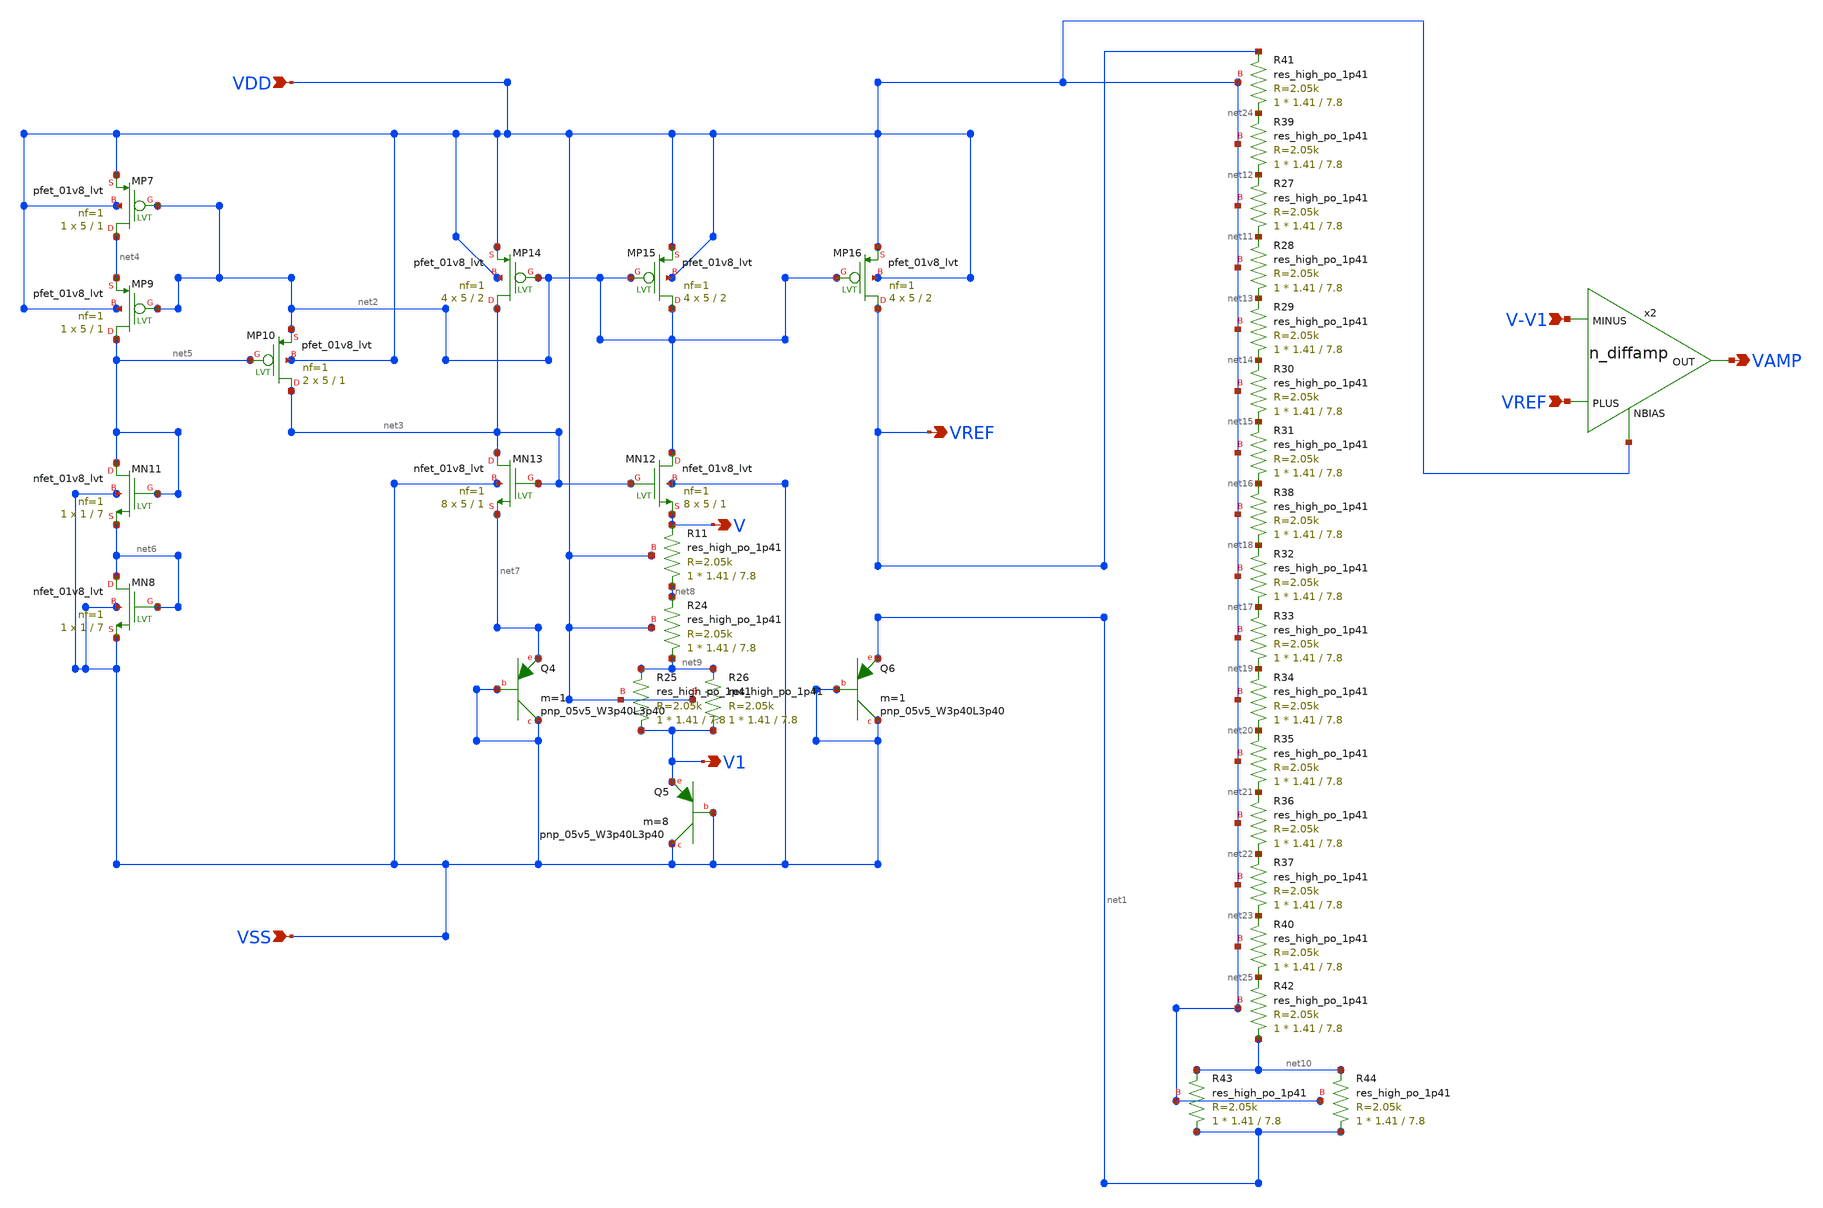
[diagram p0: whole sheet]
** sch_path: rply_project_sky130nm/design/RPLY_PROJECT_SKY130NM/RPLY_PROJECT.sch
* StefanSchippers/xschem_sky130/sky130_tests/n_diffamp.sch:
* Copyright 2021 Stefan Frederik Schippers
* Licensed under the Apache License, Version 2.0 (the "License");
**.subckt RPLY_PROJECT VDD VSS V-V1 VAMP V V1 VREF VREF
*.ipin VDD
*.ipin VSS
*.ipin V-V1
*.opin VAMP
*.opin V
*.opin V1
*.opin VREF
*.ipin VREF
XMP7 net4 net2 VDD VDD sky130_fd_pr__pfet_01v8_lvt L=1 W=5 nf=1 ad='int((nf+1)/2) * W/nf * 0.29' as='int((nf+2)/2) * W/nf * 0.29'
+ pd='2*int((nf+1)/2) * (W/nf + 0.29)' ps='2*int((nf+2)/2) * (W/nf + 0.29)' nrd='0.29 / W' nrs='0.29 / W'
+ sa=0 sb=0 sd=0 mult=1 m=1
XMN8 net6 net6 VSS VSS sky130_fd_pr__nfet_01v8_lvt L=7 W=1 nf=1 ad='int((nf+1)/2) * W/nf * 0.29' as='int((nf+2)/2) * W/nf * 0.29'
+ pd='2*int((nf+1)/2) * (W/nf + 0.29)' ps='2*int((nf+2)/2) * (W/nf + 0.29)' nrd='0.29 / W' nrs='0.29 / W'
+ sa=0 sb=0 sd=0 mult=1 m=1
XR11 net8 V VDD sky130_fd_pr__res_high_po_1p41 L=7.8 mult=1 m=1
XQ4 VSS VSS net7 sky130_fd_pr__pnp_05v5_W3p40L3p40 m=1
XMP9 net5 net2 net4 VDD sky130_fd_pr__pfet_01v8_lvt L=1 W=5 nf=1 ad='int((nf+1)/2) * W/nf * 0.29' as='int((nf+2)/2) * W/nf * 0.29'
+ pd='2*int((nf+1)/2) * (W/nf + 0.29)' ps='2*int((nf+2)/2) * (W/nf + 0.29)' nrd='0.29 / W' nrs='0.29 / W'
+ sa=0 sb=0 sd=0 mult=1 m=1
XMP10 net3 net5 net2 VDD sky130_fd_pr__pfet_01v8_lvt L=1 W=5 nf=1 ad='int((nf+1)/2) * W/nf * 0.29' as='int((nf+2)/2) * W/nf * 0.29'
+ pd='2*int((nf+1)/2) * (W/nf + 0.29)' ps='2*int((nf+2)/2) * (W/nf + 0.29)' nrd='0.29 / W' nrs='0.29 / W'
+ sa=0 sb=0 sd=0 mult=2 m=2
XMN11 net5 net5 net6 VSS sky130_fd_pr__nfet_01v8_lvt L=7 W=1 nf=1 ad='int((nf+1)/2) * W/nf * 0.29' as='int((nf+2)/2) * W/nf * 0.29'
+ pd='2*int((nf+1)/2) * (W/nf + 0.29)' ps='2*int((nf+2)/2) * (W/nf + 0.29)' nrd='0.29 / W' nrs='0.29 / W'
+ sa=0 sb=0 sd=0 mult=1 m=1
XQ5 VSS VSS V1 sky130_fd_pr__pnp_05v5_W3p40L3p40 m=8
XQ6 VSS VSS net1 sky130_fd_pr__pnp_05v5_W3p40L3p40 m=1
XMN12 net2 net3 V VSS sky130_fd_pr__nfet_01v8_lvt L=1 W=5 nf=1 ad='int((nf+1)/2) * W/nf * 0.29' as='int((nf+2)/2) * W/nf * 0.29'
+ pd='2*int((nf+1)/2) * (W/nf + 0.29)' ps='2*int((nf+2)/2) * (W/nf + 0.29)' nrd='0.29 / W' nrs='0.29 / W'
+ sa=0 sb=0 sd=0 mult=8 m=8
XMN13 net3 net3 net7 VSS sky130_fd_pr__nfet_01v8_lvt L=1 W=5 nf=1 ad='int((nf+1)/2) * W/nf * 0.29' as='int((nf+2)/2) * W/nf * 0.29'
+ pd='2*int((nf+1)/2) * (W/nf + 0.29)' ps='2*int((nf+2)/2) * (W/nf + 0.29)' nrd='0.29 / W' nrs='0.29 / W'
+ sa=0 sb=0 sd=0 mult=8 m=8
XMP14 net3 net2 VDD VDD sky130_fd_pr__pfet_01v8_lvt L=2 W=5 nf=1 ad='int((nf+1)/2) * W/nf * 0.29' as='int((nf+2)/2) * W/nf * 0.29'
+ pd='2*int((nf+1)/2) * (W/nf + 0.29)' ps='2*int((nf+2)/2) * (W/nf + 0.29)' nrd='0.29 / W' nrs='0.29 / W'
+ sa=0 sb=0 sd=0 mult=4 m=4
XMP15 net2 net2 VDD VDD sky130_fd_pr__pfet_01v8_lvt L=2 W=5 nf=1 ad='int((nf+1)/2) * W/nf * 0.29' as='int((nf+2)/2) * W/nf * 0.29'
+ pd='2*int((nf+1)/2) * (W/nf + 0.29)' ps='2*int((nf+2)/2) * (W/nf + 0.29)' nrd='0.29 / W' nrs='0.29 / W'
+ sa=0 sb=0 sd=0 mult=4 m=4
XMP16 VREF net2 VDD VDD sky130_fd_pr__pfet_01v8_lvt L=2 W=5 nf=1 ad='int((nf+1)/2) * W/nf * 0.29' as='int((nf+2)/2) * W/nf * 0.29'
+ pd='2*int((nf+1)/2) * (W/nf + 0.29)' ps='2*int((nf+2)/2) * (W/nf + 0.29)' nrd='0.29 / W' nrs='0.29 / W'
+ sa=0 sb=0 sd=0 mult=4 m=4
XR24 net9 net8 VDD sky130_fd_pr__res_high_po_1p41 L=7.8 mult=1 m=1
XR25 V1 net9 VDD sky130_fd_pr__res_high_po_1p41 L=7.8 mult=1 m=1
XR26 V1 net9 VDD sky130_fd_pr__res_high_po_1p41 L=7.8 mult=1 m=1
XR27 net11 net12 VDD sky130_fd_pr__res_high_po_1p41 L=7.8 mult=1 m=1
XR28 net13 net11 VDD sky130_fd_pr__res_high_po_1p41 L=7.8 mult=1 m=1
XR29 net14 net13 VDD sky130_fd_pr__res_high_po_1p41 L=7.8 mult=1 m=1
XR30 net15 net14 VDD sky130_fd_pr__res_high_po_1p41 L=7.8 mult=1 m=1
XR31 net16 net15 VDD sky130_fd_pr__res_high_po_1p41 L=7.8 mult=1 m=1
XR32 net17 net18 VDD sky130_fd_pr__res_high_po_1p41 L=7.8 mult=1 m=1
XR33 net19 net17 VDD sky130_fd_pr__res_high_po_1p41 L=7.8 mult=1 m=1
XR34 net20 net19 VDD sky130_fd_pr__res_high_po_1p41 L=7.8 mult=1 m=1
XR35 net21 net20 VDD sky130_fd_pr__res_high_po_1p41 L=7.8 mult=1 m=1
XR36 net22 net21 VDD sky130_fd_pr__res_high_po_1p41 L=7.8 mult=1 m=1
XR37 net23 net22 VDD sky130_fd_pr__res_high_po_1p41 L=7.8 mult=1 m=1
XR38 net18 net16 VDD sky130_fd_pr__res_high_po_1p41 L=7.8 mult=1 m=1
XR39 net12 net24 VDD sky130_fd_pr__res_high_po_1p41 L=7.8 mult=1 m=1
XR40 net25 net23 VDD sky130_fd_pr__res_high_po_1p41 L=7.8 mult=1 m=1
XR41 net24 VREF VDD sky130_fd_pr__res_high_po_1p41 L=7.8 mult=1 m=1
XR42 net10 net25 VDD sky130_fd_pr__res_high_po_1p41 L=7.8 mult=1 m=1
XR43 net1 net10 VDD sky130_fd_pr__res_high_po_1p41 L=7.8 mult=1 m=1
XR44 net1 net10 VDD sky130_fd_pr__res_high_po_1p41 L=7.8 mult=1 m=1
x2 VAMP V-V1 VREF VDD n_diffamp
**.ends

* expanding   symbol:  sky130_tests/n_diffamp.sym # of pins=4
** sym_path: sky130_tests/n_diffamp.sym
** sch_path: sky130_tests/n_diffamp.sch
.subckt n_diffamp OUT MINUS PLUS NBIAS
*.ipin PLUS
*.ipin MINUS
*.opin OUT
*.ipin NBIAS
XM1 net1 PLUS S GND sky130_fd_pr__nfet_01v8_lvt L=0.3 W=2 nf=1 ad='int((1 + 1)/2) * 2 / 1 * 0.29' as='int((1 + 2)/2) * 2 / 1 * 0.29'
+ pd='2*int((1 + 1)/2) * (2 / 1 + 0.29)' ps='2*int((1 + 2)/2) * (2 / 1 + 0.29)' nrd='0.29 / 2 ' nrs='0.29 / 2 '
+ sa=0 sb=0 sd=0 mult=1 m=1
XM2 OUT MINUS S GND sky130_fd_pr__nfet_01v8_lvt L=0.3 W=2 nf=1 ad='int((1 + 1)/2) * 2 / 1 * 0.29' as='int((1 + 2)/2) * 2 / 1 * 0.29'
+ pd='2*int((1 + 1)/2) * (2 / 1 + 0.29)' ps='2*int((1 + 2)/2) * (2 / 1 + 0.29)' nrd='0.29 / 2 ' nrs='0.29 / 2 '
+ sa=0 sb=0 sd=0 mult=1 m=1
XM3 OUT net1 VDD VDD sky130_fd_pr__pfet_01v8_lvt L=0.8 W=4 nf=1 ad='int((1 + 1)/2) * 4 / 1 * 0.29' as='int((1 + 2)/2) * 4 / 1 * 0.29'
+ pd='2*int((1 + 1)/2) * (4 / 1 + 0.29)' ps='2*int((1 + 2)/2) * (4 / 1 + 0.29)' nrd='0.29 / 4 ' nrs='0.29 / 4 '
+ sa=0 sb=0 sd=0 mult=1 m=1
XM4 net1 net1 VDD VDD sky130_fd_pr__pfet_01v8_lvt L=0.8 W=4 nf=1 ad='int((1 + 1)/2) * 4 / 1 * 0.29' as='int((1 + 2)/2) * 4 / 1 * 0.29'
+ pd='2*int((1 + 1)/2) * (4 / 1 + 0.29)' ps='2*int((1 + 2)/2) * (4 / 1 + 0.29)' nrd='0.29 / 4 ' nrs='0.29 / 4 '
+ sa=0 sb=0 sd=0 mult=1 m=1
XM5 net2 NBIAS GND GND sky130_fd_pr__nfet_01v8 L=2 W=0.7 nf=1 ad='int((nf+1)/2) * W/nf * 0.29' as='int((nf+2)/2) * W/nf * 0.29'
+ pd='2*int((nf+1)/2) * (W/nf + 0.29)' ps='2*int((nf+2)/2) * (W/nf + 0.29)' nrd='0.29 / W' nrs='0.29 / W'
+ sa=0 sb=0 sd=0 mult=1 m=1
XR1 GND S GND sky130_fd_pr__res_xhigh_po_0p35 L=50 mult=1 m=1
V5 S net2 0
.save i(v5)
.ends

.GLOBAL GND
.GLOBAL VDD
.end
